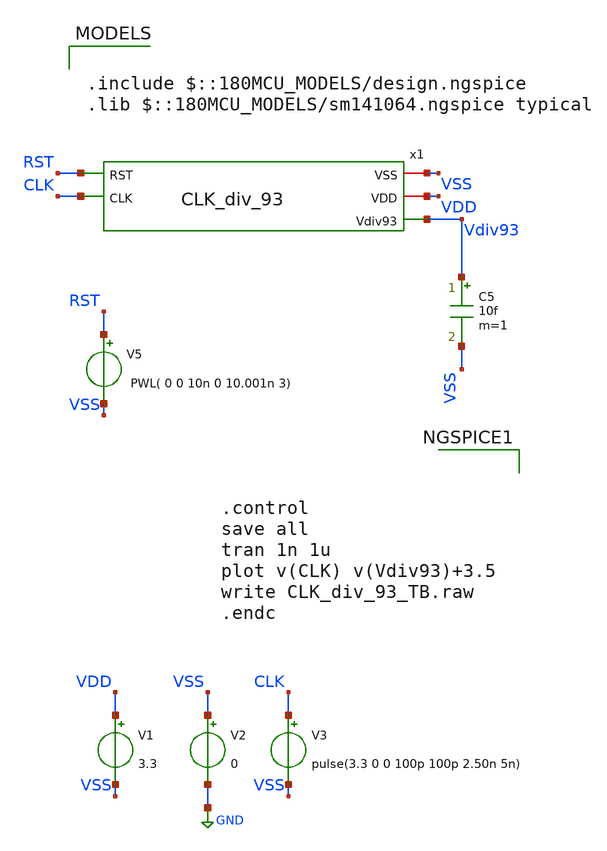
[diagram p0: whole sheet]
** sch_path: Clock_Generator_PAKISTAN_02/xschem/CLK_div_93_TB.sch
**.subckt CLK_div_93_TB
V1 VDD VSS 3.3
V2 VSS GND 0
V3 CLK VSS pulse(3.3 0 0 100p 100p 2.50n 5n)
C5 Vdiv93 VSS 10f m=1
x1 VSS VDD Vdiv93 RST CLK CLK_div_93
V5 RST VSS PWL( 0 0 10n 0 10.001n 3)
**** begin user architecture code

.include $::180MCU_MODELS/design.ngspice
.lib $::180MCU_MODELS/sm141064.ngspice typical




.control
save all
tran 1n 1u
plot v(CLK) v(Vdiv93)+3.5
write CLK_div_93_TB.raw
.endc


**** end user architecture code
**.ends
.GLOBAL GND
.end
